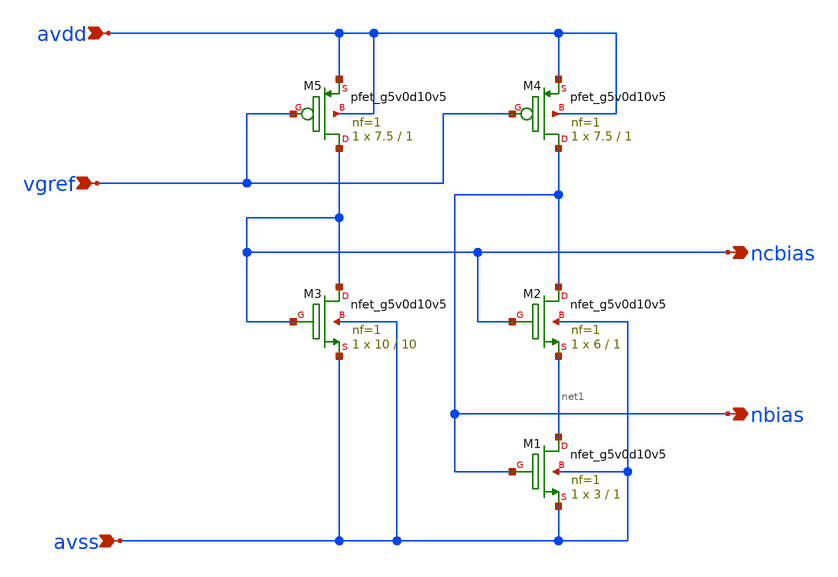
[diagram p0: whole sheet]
** sch_path: xschem/n_ibias_mirror.sch
**.subckt n_ibias_mirror avss avdd nbias ncbias vgref
*.ipin avss
*.ipin avdd
*.opin nbias
*.opin ncbias
*.ipin vgref
XM1 net1 nbias avss avss sky130_fd_pr__nfet_g5v0d10v5 L=1 W=3 nf=1 ad='int((nf+1)/2) * W/nf * 0.29' as='int((nf+2)/2) * W/nf * 0.29'
+ pd='2*int((nf+1)/2) * (W/nf + 0.29)' ps='2*int((nf+2)/2) * (W/nf + 0.29)' nrd='0.29 / W' nrs='0.29 / W'
+ sa=0 sb=0 sd=0 mult=1 m=1
XM2 nbias ncbias net1 avss sky130_fd_pr__nfet_g5v0d10v5 L=1 W=6 nf=1 ad='int((nf+1)/2) * W/nf * 0.29'
+ as='int((nf+2)/2) * W/nf * 0.29' pd='2*int((nf+1)/2) * (W/nf + 0.29)' ps='2*int((nf+2)/2) * (W/nf + 0.29)'
+ nrd='0.29 / W' nrs='0.29 / W' sa=0 sb=0 sd=0 mult=1 m=1
XM3 ncbias ncbias avss avss sky130_fd_pr__nfet_g5v0d10v5 L=10 W=10 nf=1 ad='int((nf+1)/2) * W/nf * 0.29'
+ as='int((nf+2)/2) * W/nf * 0.29' pd='2*int((nf+1)/2) * (W/nf + 0.29)' ps='2*int((nf+2)/2) * (W/nf + 0.29)'
+ nrd='0.29 / W' nrs='0.29 / W' sa=0 sb=0 sd=0 mult=1 m=1
XM4 nbias vgref avdd avdd sky130_fd_pr__pfet_g5v0d10v5 L=1 W=7.5 nf=1 ad='int((nf+1)/2) * W/nf * 0.29'
+ as='int((nf+2)/2) * W/nf * 0.29' pd='2*int((nf+1)/2) * (W/nf + 0.29)' ps='2*int((nf+2)/2) * (W/nf + 0.29)'
+ nrd='0.29 / W' nrs='0.29 / W' sa=0 sb=0 sd=0 mult=1 m=1
XM5 ncbias vgref avdd avdd sky130_fd_pr__pfet_g5v0d10v5 L=1 W=7.5 nf=1 ad='int((nf+1)/2) * W/nf * 0.29'
+ as='int((nf+2)/2) * W/nf * 0.29' pd='2*int((nf+1)/2) * (W/nf + 0.29)' ps='2*int((nf+2)/2) * (W/nf + 0.29)'
+ nrd='0.29 / W' nrs='0.29 / W' sa=0 sb=0 sd=0 mult=1 m=1
**.ends
.end
